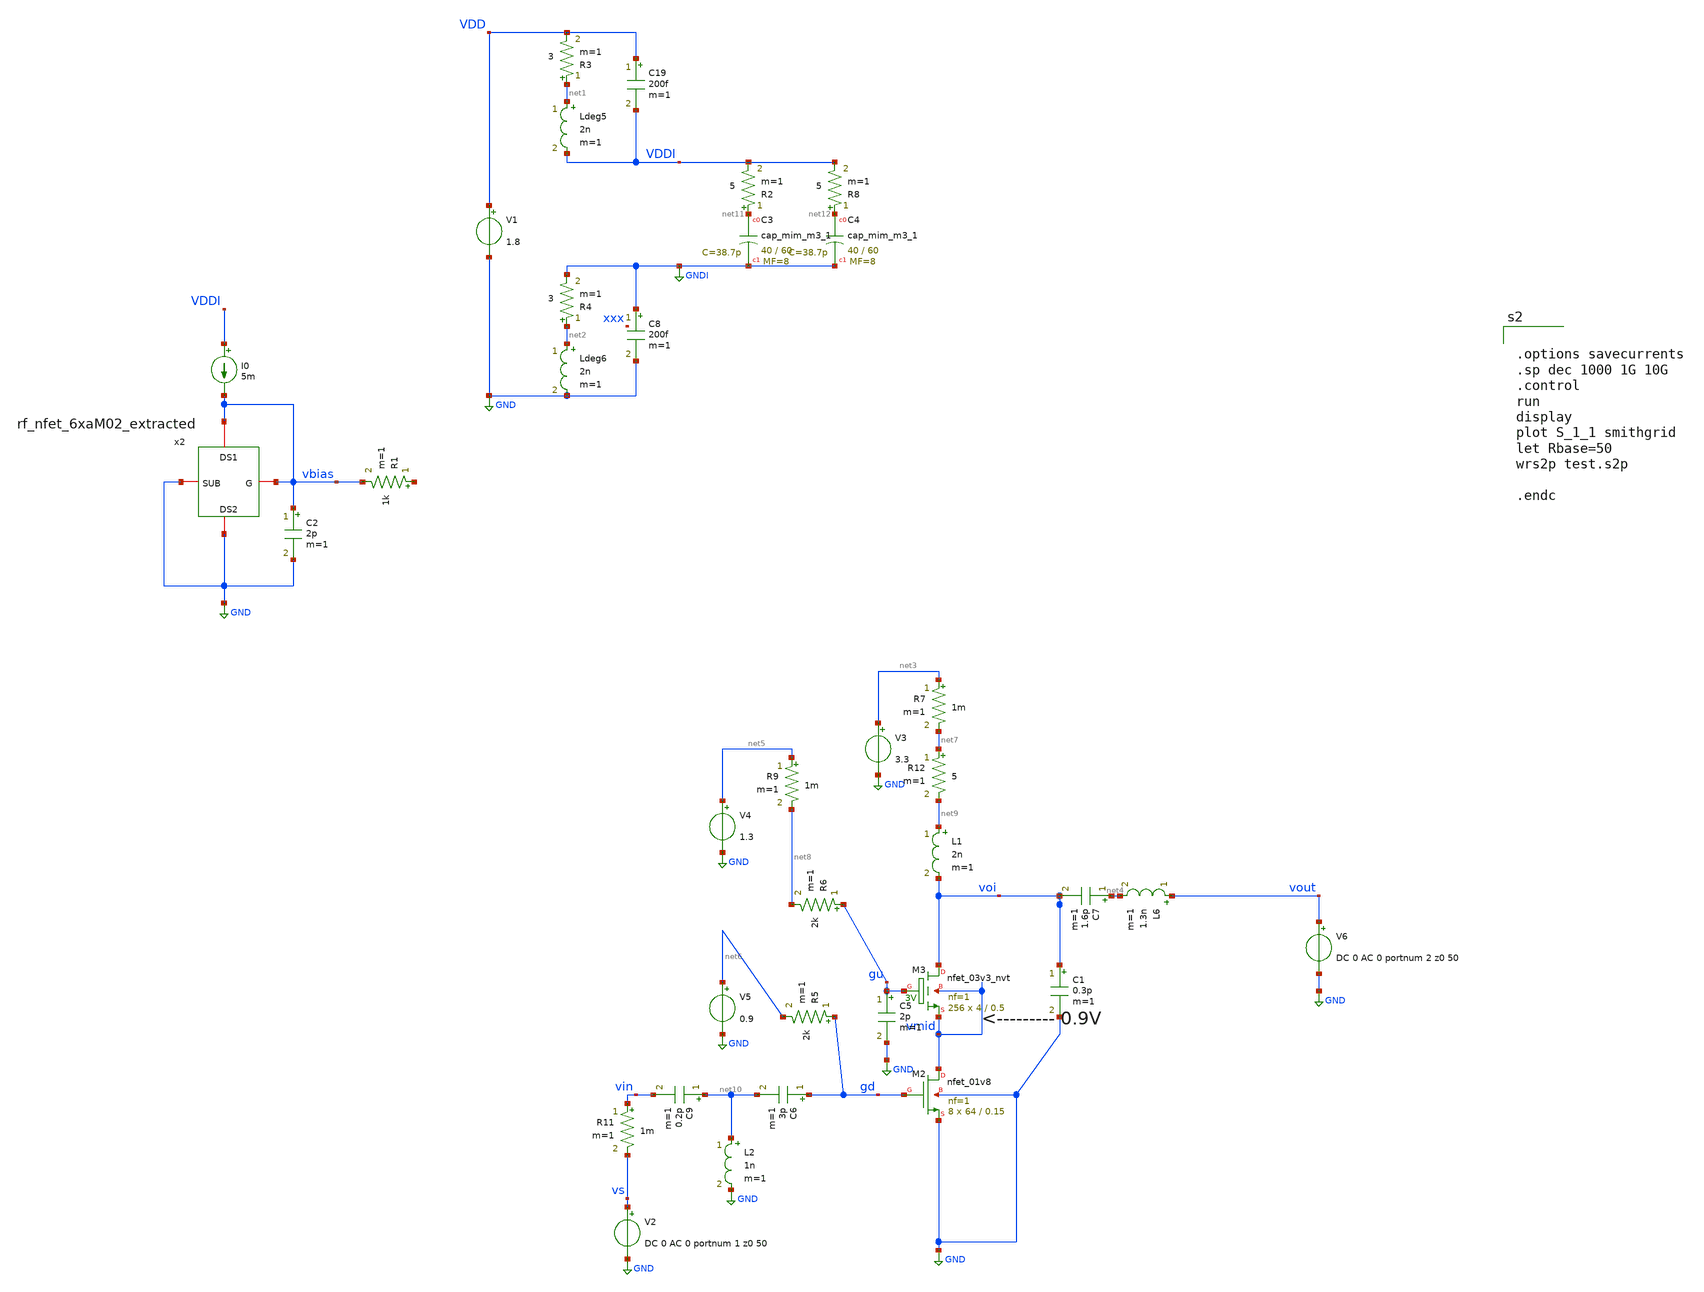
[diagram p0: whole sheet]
** sch_path: xschem/2stack_2_sp.sch
**.subckt 2stack_2_sp
V1 VDD GND 1.8
Ldeg5 net1 VDDI 2n m=1
R3 net1 VDD 3 m=1
Ldeg6 net2 GND 2n m=1
R4 net2 GNDI 3 m=1
XC3 net11 GNDI sky130_fd_pr__cap_mim_m3_1 W=40 L=60 MF=8 m=8
C8 GNDI GND 200f m=1
C19 VDD VDDI 200f m=1
R2 net11 VDDI 5 m=1
XC4 net12 GNDI sky130_fd_pr__cap_mim_m3_1 W=40 L=60 MF=8 m=8
R8 net12 VDDI 5 m=1
V2 vs GND DC 0 AC 0 portnum 1 z0 50
x2 vbias vbias GND GND rf_nfet_6xaM02_extracted
I0 VDDI vbias 5m
R1 net13 vbias 1k m=1
C2 vbias GND 2p m=1
V3 net3 GND 3.3
L1 net9 voi 2n m=1
L6 vout net4 1.3n m=1
C7 net4 voi 1.6p m=1
C1 voi GND 0.3p m=1
V4 net5 GND 1.3
R5 gd net6 2k m=1
V5 net6 GND 0.9
XM3 voi gu vmid vmid sky130_fd_pr__nfet_03v3_nvt L=0.5 W=4 nf=1 ad='int((nf+1)/2) * W/nf * 0.29' as='int((nf+2)/2) * W/nf * 0.29'
+ pd='2*int((nf+1)/2) * (W/nf + 0.29)' ps='2*int((nf+2)/2) * (W/nf + 0.29)' nrd='0.29 / W' nrs='0.29 / W'
+ sa=0 sb=0 sd=0 mult=256 m=256
R6 gu net8 2k m=1
C5 gu GND 2p m=1
R7 net3 net7 1m m=1
R9 net5 net8 1m m=1
XM2 vmid gd GND GND sky130_fd_pr__nfet_01v8 L=0.15 W=64 nf=1 ad='int((nf+1)/2) * W/nf * 0.29' as='int((nf+2)/2) * W/nf * 0.29'
+ pd='2*int((nf+1)/2) * (W/nf + 0.29)' ps='2*int((nf+2)/2) * (W/nf + 0.29)' nrd='0.29 / W' nrs='0.29 / W'
+ sa=0 sb=0 sd=0 mult=8 m=8
R11 vin vs 1m m=1
R12 net7 net9 5 m=1
V6 vout GND DC 0 AC 0 portnum 2 z0 50
C6 gd net10 3p m=1
C9 net10 vin 0.2p m=1
L2 net10 GND 1n m=1
**** begin user architecture code
.lib $::SKYWATER_MODELS/sky130.lib.spice tt
* .include $::PDKPATH/libs.ref/sky130_fd_sc_hvl/spice/sky130_fd_sc_hvl.spice



.options savecurrents
.sp dec 1000 1G 10G
.control
run
display
plot S_1_1 smithgrid
let Rbase=50
wrs2p test.s2p

.endc


**** end user architecture code
**.ends

* expanding   symbol:  rf_nfet_6xaM02_extracted.sym # of pins=4
** sym_path: xschem/rf_nfet_6xaM02_extracted.sym
** sch_path: xschem/rf_nfet_6xaM02_extracted.sch
.subckt rf_nfet_6xaM02_extracted G DS1 DS2 SUB
*.iopin G
*.iopin DS1
*.iopin DS2
*.iopin SUB
**** begin user architecture code


* Extraction of 6xaM02 (12 finger) Transistors
* wt=60um, L=0.15um
.subckt NFET_extract_1 SD1 G2 SD2 SUB

* .subckt sky130_fd_pr__rf_nfet_01v8_aM02W5p00L0p15 DRAIN GATE SOURCE SUBSTRATE
*  X0 DRAIN GATE SOURCE SUBSTRATE sky130_fd_pr__nfet_01v8 ad=1.414e+12p pd=1.066e+07u as=2.828e+12p
*+ ps=2.132e+07u w=5.05e+06u l=150000u
*  X1 SOURCE GATE DRAIN SUBSTRATE sky130_fd_pr__nfet_01v8 ad=0p pd=0u as=0p ps=0u w=5.05e+06u
*+ l=150000u
*  C0 SOURCE DRAIN 3.73fF
*  C1 SOURCE SUBSTRATE 2.58fF
* .ends

X0 SD1 G2 SD2 SUB sky130_fd_pr__nfet_01v8 ad=0p pd=0u as=0p ps=0u w=5.05e+06u l=150000u
X1 SD1 G2 SD2 SUB sky130_fd_pr__nfet_01v8 ad=0p pd=0u as=0p ps=0u w=5.05e+06u l=150000u
X2 SD2 G2 SD1 SUB sky130_fd_pr__nfet_01v8 ad=0p pd=0u as=0p ps=0u w=5.05e+06u l=150000u
X3 SD2 G2 SD1 SUB sky130_fd_pr__nfet_01v8 ad=0p pd=0u as=0p ps=0u w=5.05e+06u l=150000u
X4 SD1 G2 SD2 SUB sky130_fd_pr__nfet_01v8 ad=0p pd=0u as=0p ps=0u w=5.05e+06u l=150000u
X5 SD1 G2 SD2 SUB sky130_fd_pr__nfet_01v8 ad=0p pd=0u as=0p ps=0u w=5.05e+06u l=150000u
X6 SD2 G2 SD1 SUB sky130_fd_pr__nfet_01v8 ad=0p pd=0u as=0p ps=0u w=5.05e+06u l=150000u
X7 SD2 G2 SD1 SUB sky130_fd_pr__nfet_01v8 ad=0p pd=0u as=0p ps=0u w=5.05e+06u l=150000u
X8 SD1 G2 SD2 SUB sky130_fd_pr__nfet_01v8 ad=0p pd=0u as=0p ps=0u w=5.05e+06u l=150000u
X9 SD1 G2 SD2 SUB sky130_fd_pr__nfet_01v8 ad=0p pd=0u as=0p ps=0u w=5.05e+06u l=150000u
X10 SD2 G2 SD1 SUB sky130_fd_pr__nfet_01v8 ad=0p pd=0u as=0p ps=0u w=5.05e+06u l=150000u
X11 SD2 G2 SD1 SUB sky130_fd_pr__nfet_01v8 ad=0p pd=0u as=0p ps=0u w=5.05e+06u l=150000u
C0 SD2 G2 3.50fF
C1 SUB SD1 3.01fF
C2 G2 SD1 4.50fF
C3 G2 SUB 2.28fF
C4 SD2 SD1 30.48fF
C5 G2 SUB 3.11fF
C6 SD1 SUB 6.76fF

* C0 B G 2.85fF
* C1 S D 22.23fF
* C2 G D 5.77fF
* C3 S G 7.53fF
* Xnfet_3x_2_0/sky130_fd_pr__rf_nfet_01v8_aM02W5p00L0p15_0 D G S B
*+ sky130_fd_pr__rf_nfet_01v8_aM02W5p00L0p15
* Xnfet_3x_2_0/sky130_fd_pr__rf_nfet_01v8_aM02W5p00L0p15_1 D G S B
*+ sky130_fd_pr__rf_nfet_01v8_aM02W5p00L0p15
* Xnfet_3x_2_0/sky130_fd_pr__rf_nfet_01v8_aM02W5p00L0p15_2 D G S B
*+ sky130_fd_pr__rf_nfet_01v8_aM02W5p00L0p15
* Xnfet_3x_2_1/sky130_fd_pr__rf_nfet_01v8_aM02W5p00L0p15_0 D G S B
*+ sky130_fd_pr__rf_nfet_01v8_aM02W5p00L0p15
* Xnfet_3x_2_1/sky130_fd_pr__rf_nfet_01v8_aM02W5p00L0p15_1 D G S B
*+ sky130_fd_pr__rf_nfet_01v8_aM02W5p00L0p15
* Xnfet_3x_2_1/sky130_fd_pr__rf_nfet_01v8_aM02W5p00L0p15_2 D G S B
*+ sky130_fd_pr__rf_nfet_01v8_aM02W5p00L0p15
* C4 S B 13.70fF
* C5 G B 3.35fF

.ends

XM0 DS1 G DS2 SUB NFET_extract_1


**** end user architecture code
.ends

.GLOBAL GND
.GLOBAL GNDI
.end
